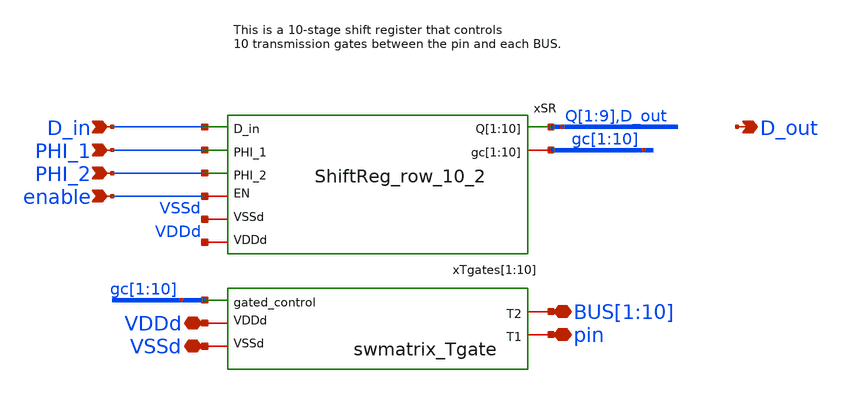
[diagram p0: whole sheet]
** sch_path: swmatrix_row_10/swmatrix_row_10.sch
**.subckt swmatrix_row_10 pin PHI_2 PHI_1
*+ BUS[1],BUS[2],BUS[3],BUS[4],BUS[5],BUS[6],BUS[7],BUS[8],BUS[9],BUS[10] D_in D_out VDDd VSSd enable
*.iopin pin
*.ipin PHI_2
*.ipin PHI_1
*.iopin BUS[1],BUS[2],BUS[3],BUS[4],BUS[5],BUS[6],BUS[7],BUS[8],BUS[9],BUS[10]
*.ipin D_in
*.opin D_out
*.iopin VDDd
*.iopin VSSd
*.ipin enable
xSR D_in Q[1] Q[2] Q[3] Q[4] Q[5] Q[6] Q[7] Q[8] Q[9] D_out gc[1] gc[2] gc[3] gc[4] gc[5] gc[6]
+ gc[7] gc[8] gc[9] gc[10] PHI_1 PHI_2 enable VDDd VSSd ShiftReg_row_10_2
xTgates[1] gc[1] BUS[1] pin VSSd VDDd swmatrix_Tgate
xTgates[2] gc[2] BUS[2] pin VSSd VDDd swmatrix_Tgate
xTgates[3] gc[3] BUS[3] pin VSSd VDDd swmatrix_Tgate
xTgates[4] gc[4] BUS[4] pin VSSd VDDd swmatrix_Tgate
xTgates[5] gc[5] BUS[5] pin VSSd VDDd swmatrix_Tgate
xTgates[6] gc[6] BUS[6] pin VSSd VDDd swmatrix_Tgate
xTgates[7] gc[7] BUS[7] pin VSSd VDDd swmatrix_Tgate
xTgates[8] gc[8] BUS[8] pin VSSd VDDd swmatrix_Tgate
xTgates[9] gc[9] BUS[9] pin VSSd VDDd swmatrix_Tgate
xTgates[10] gc[10] BUS[10] pin VSSd VDDd swmatrix_Tgate
**.ends
.end
